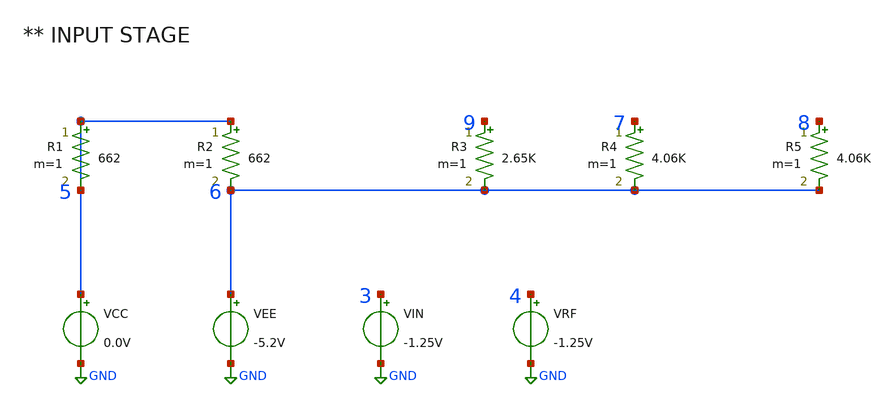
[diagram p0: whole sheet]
** sch_path: data/sch/aicas_eclinv.sch
**.subckt aicas_eclinv
VCC 5 GND 0.0V
VEE 6 GND -5.2V
VIN 3 GND -1.25V
VRF 4 GND -1.25V
R1 5 5 662 m=1
R2 5 6 662 m=1
R3 9 6 2.65K m=1
R4 7 6 4.06K m=1
R5 8 6 4.06K m=1
**.ends
.GLOBAL GND
.end
